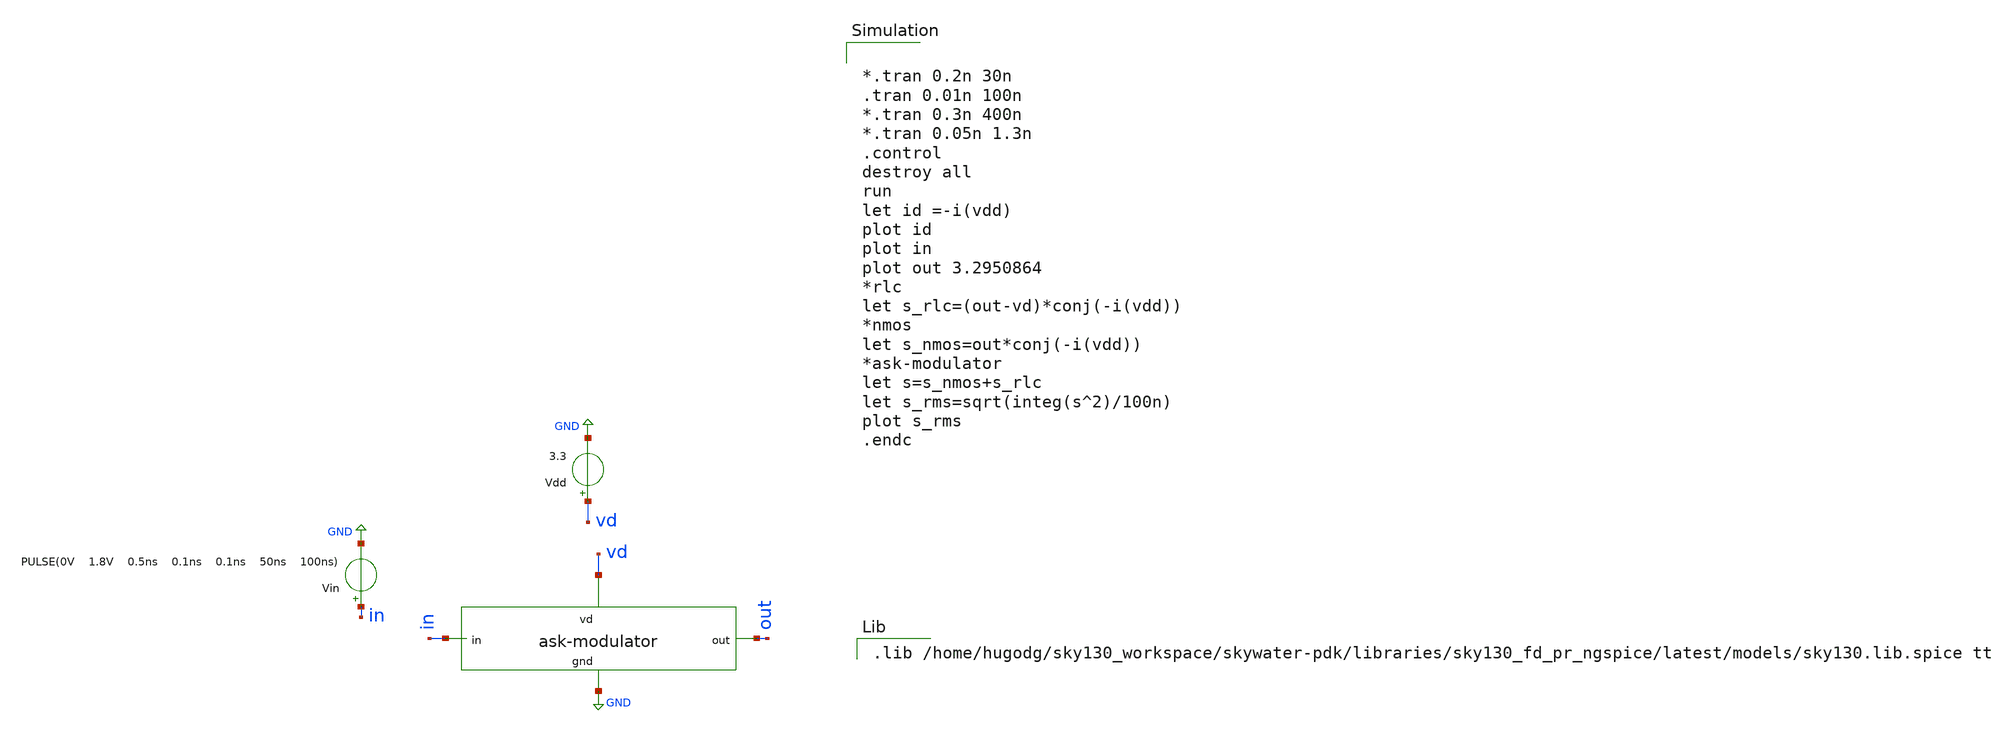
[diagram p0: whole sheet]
** sch_path: ask_modulator/xschem/ask-modulator_tb-tran.sch
**.subckt ask-modulator_tb-tran
Vdd vd GND 3.3
Vin in GND PULSE(0V 1.8V 0.5ns 0.1ns 0.1ns 50ns 100ns)
x1 vd out in GND ask-modulator
**** begin user architecture code


*.tran 0.2n 30n
.tran 0.01n 100n
*.tran 0.3n 400n
*.tran 0.05n 1.3n
.control
destroy all
run
let id =-i(vdd)
plot id
plot in
plot out 3.2950864
*rlc
let s_rlc=(out-vd)*conj(-i(vdd))
*nmos
let s_nmos=out*conj(-i(vdd))
*ask-modulator
let s=s_nmos+s_rlc
let s_rms=sqrt(integ(s^2)/100n)
plot s_rms
.endc


.lib /home/hugodg/sky130_workspace/skywater-pdk/libraries/sky130_fd_pr_ngspice/latest/models/sky130.lib.spice tt

**** end user architecture code
**.ends
.GLOBAL GND
.end
